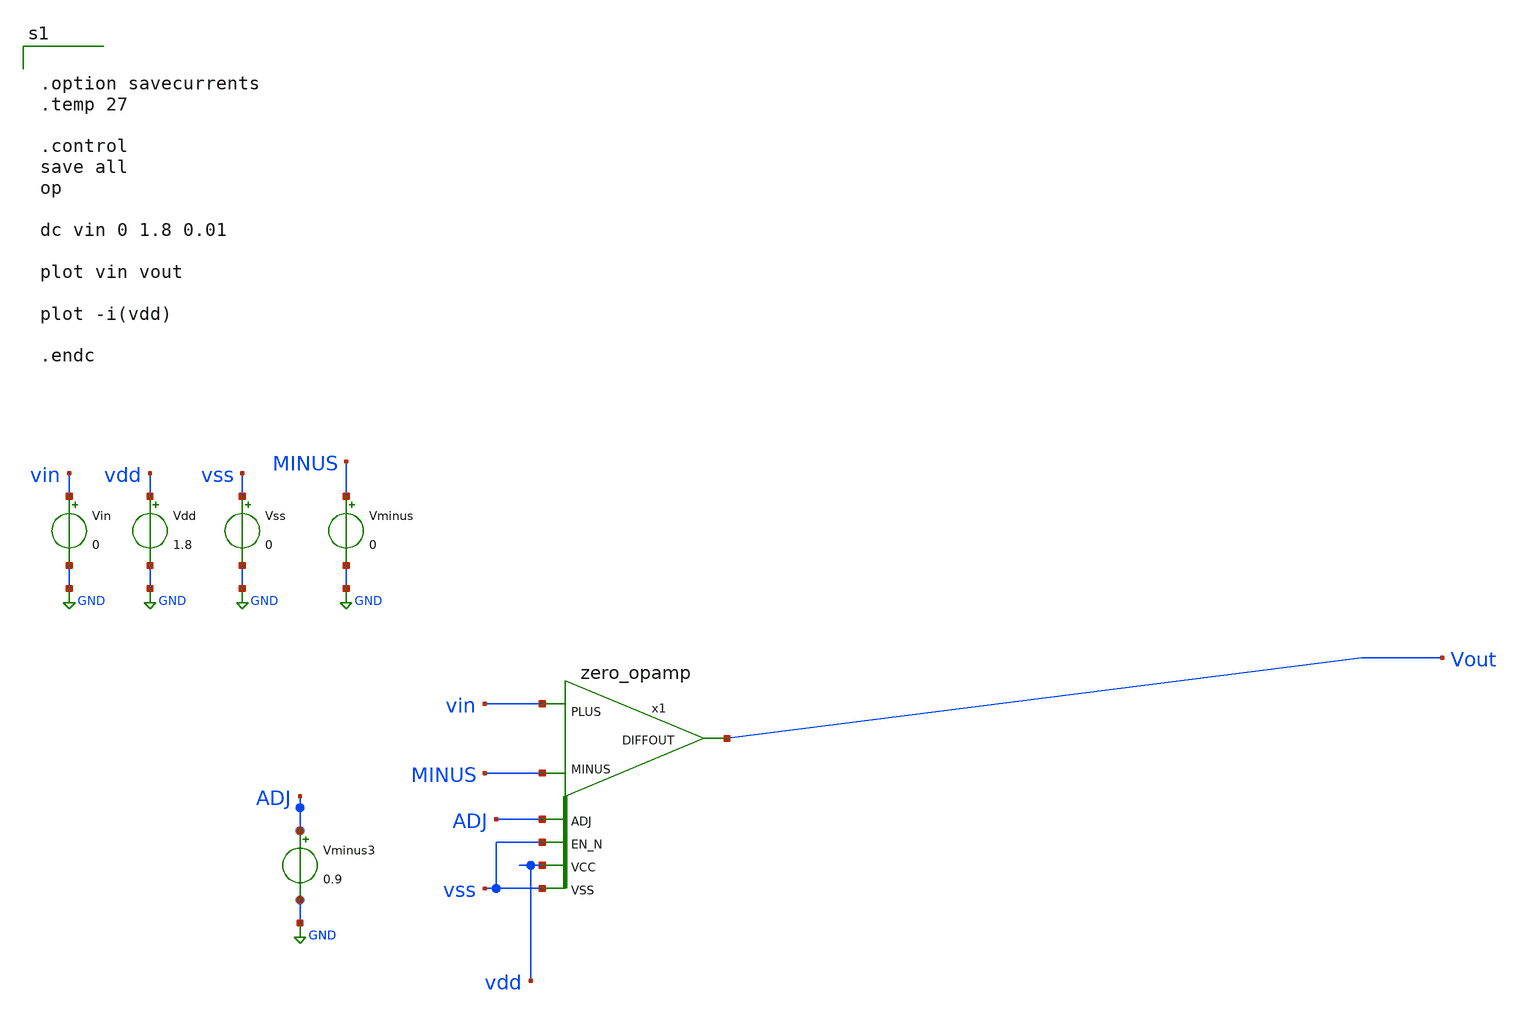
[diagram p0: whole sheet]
** sch_path: Schematic/LNA.sch
* StefanSchippers/xschem_sky130/sky130_tests/zero_opamp.sch:
* Copyright 2021 Stefan Frederik Schippers
* Licensed under the Apache License, Version 2.0 (the "License");
**.subckt LNA
Vin vin GND 0
Vdd vdd GND 1.8
Vminus MINUS GND 0
Vss vss GND 0
x1 vss MINUS vin Vout vdd vss ADJ zero_opamp
Vminus3 ADJ GND 0.9
**** begin user architecture code

** opencircuitdesign pdks install
.lib $::SKYWATER_MODELS/sky130.lib.spice tt




.option savecurrents
.temp 27

.control
save all
op

dc vin 0 1.8 0.01

plot vin vout

plot -i(vdd)

.endc

**** end user architecture code
**.ends

* expanding   symbol:  sky130_tests/zero_opamp.sym # of pins=7
** sym_path: sky130_tests/zero_opamp.sym
** sch_path: sky130_tests/zero_opamp.sch
.subckt zero_opamp EN_N MINUS PLUS DIFFOUT VCC VSS ADJ
*.ipin PLUS
*.ipin MINUS
*.ipin EN_N
*.ipin VSS
*.ipin VCC
*.opin DIFFOUT
*.ipin ADJ
C6 G1 0 2f m=1
XM4 net9 EN_N VCC VCC sky130_fd_pr__pfet_01v8 L=8 W=2 nf=1 ad='W * 0.29' as='W * 0.29' pd='W + 2 * 0.29'
+ ps='W + 2 * 0.29' nrd=0 nrs=0 sa=0 sb=0 sd=0 mult=1 m=1
XM18 G2 G2 net7 VSS sky130_fd_pr__nfet_01v8_lvt L=4 W=2 nf=1 ad='W * 0.29' as='W * 0.29' pd='2*(W + 0.29)'
+ ps='2*(W + 0.29)' nrd=0 nrs=0 sa=0 sb=0 sd=0 mult=1 m=1
XM2 G1 G1 net8 VSS sky130_fd_pr__nfet_01v8_lvt L=4 W=2 nf=1 ad='W * 0.29' as='W * 0.29' pd='2*(W + 0.29)'
+ ps='2*(W + 0.29)' nrd=0 nrs=0 sa=0 sb=0 sd=0 mult=1 m=1
XMR G2 PLUS net10 VCC sky130_fd_pr__pfet_01v8_lvt L=2 W=8 nf=1 ad='W * 0.29' as='W * 0.29' pd='2*(W + 0.29)'
+ ps='2*(W + 0.29)' nrd=0 nrs=0 sa=0 sb=0 sd=0 mult=1 m=1
XML G1 MINUS net11 VCC sky130_fd_pr__pfet_01v8_lvt L=2 W=8 nf=1 ad='W * 0.29' as='W * 0.29' pd='2*(W + 0.29)'
+ ps='2*(W + 0.29)' nrd=0 nrs=0 sa=0 sb=0 sd=0 mult=1 m=1
v1 SP net11 0
.save i(v1)
C4 SP 0 2f m=1
C1 G2 0 2f m=1
C5 DIFFOUT 0 4f m=1
XM6 DIFFOUT G2 net1 VSS sky130_fd_pr__nfet_01v8_lvt L=4 W=2 nf=1 ad='W * 0.29' as='W * 0.29' pd='2*(W + 0.29)'
+ ps='2*(W + 0.29)' nrd=0 nrs=0 sa=0 sb=0 sd=0 mult=1 m=1
v2 SP net10 0
.save i(v2)
v4 net1 VSS 0
.save i(v4)
v6 net9 SP 0
.save i(v6)
XM7 DIFFOUT EN_N VSS VSS sky130_fd_pr__nfet_01v8 L=0.15 W=0.5 nf=1 ad='W * 0.29' as='W * 0.29' pd='2*(W + 0.29)'
+ ps='2*(W + 0.29)' nrd=0 nrs=0 sa=0 sb=0 sd=0 mult=1 m=1
XM46 net12 EN_N VCC VCC sky130_fd_pr__pfet_01v8 L=0.15 W=5 nf=1 ad='W * 0.29' as='W * 0.29' pd='W + 2 * 0.29'
+ ps='W + 2 * 0.29' nrd=0 nrs=0 sa=0 sb=0 sd=0 mult=1 m=1
v17 net12 net3 0
.save i(v17)
XM12 net2 G1 VSS VSS sky130_fd_pr__nfet_01v8_lvt L=4 W=2 nf=1 ad='W * 0.29' as='W * 0.29' pd='2*(W + 0.29)'
+ ps='2*(W + 0.29)' nrd=0 nrs=0 sa=0 sb=0 sd=0 mult=1 m=1
XM54 net2 net2 net3 VCC sky130_fd_pr__pfet_01v8_lvt L=4 W=4 nf=1 ad='W * 0.29' as='W * 0.29' pd='2*(W + 0.29)'
+ ps='2*(W + 0.29)' nrd=0 nrs=0 sa=0 sb=0 sd=0 mult=1 m=1
XM5 DIFFOUT net2 net3 VCC sky130_fd_pr__pfet_01v8_lvt L=4 W=4 nf=1 ad='W * 0.29' as='W * 0.29' pd='2*(W + 0.29)'
+ ps='2*(W + 0.29)' nrd=0 nrs=0 sa=0 sb=0 sd=0 mult=1 m=1
XM8 net5 ADJ net4 VCC sky130_fd_pr__pfet_01v8_lvt L=1 W=1 nf=1 ad='W * 0.29' as='W * 0.29' pd='W + 2 * 0.29'
+ ps='W + 2 * 0.29' nrd=0 nrs=0 sa=0 sb=0 sd=0 mult=1 m=1
XM9 net5 ADJ net6 VSS sky130_fd_pr__nfet_01v8 L=1 W=0.5 nf=1 ad='W * 0.29' as='W * 0.29' pd='W + 2 * 0.29'
+ ps='W + 2 * 0.29' nrd=0 nrs=0 sa=0 sb=0 sd=0 mult=1 m=1
XM10 net6 VCC VSS VSS sky130_fd_pr__nfet_01v8 L=8 W=0.5 nf=1 ad='W * 0.29' as='W * 0.29' pd='2*(W + 0.29)'
+ ps='2*(W + 0.29)' nrd=0 nrs=0 sa=0 sb=0 sd=0 mult=1 m=1
XM1 net4 EN_N VCC VCC sky130_fd_pr__pfet_01v8 L=8 W=1 nf=1 ad='W * 0.29' as='W * 0.29' pd='W + 2 * 0.29'
+ ps='W + 2 * 0.29' nrd=0 nrs=0 sa=0 sb=0 sd=0 mult=1 m=1
v3 net5 G1 0
.save i(v3)
v5 net7 VSS 0
.save i(v5)
v7 net8 VSS 0
.save i(v7)
.ends

.GLOBAL GND
.end
